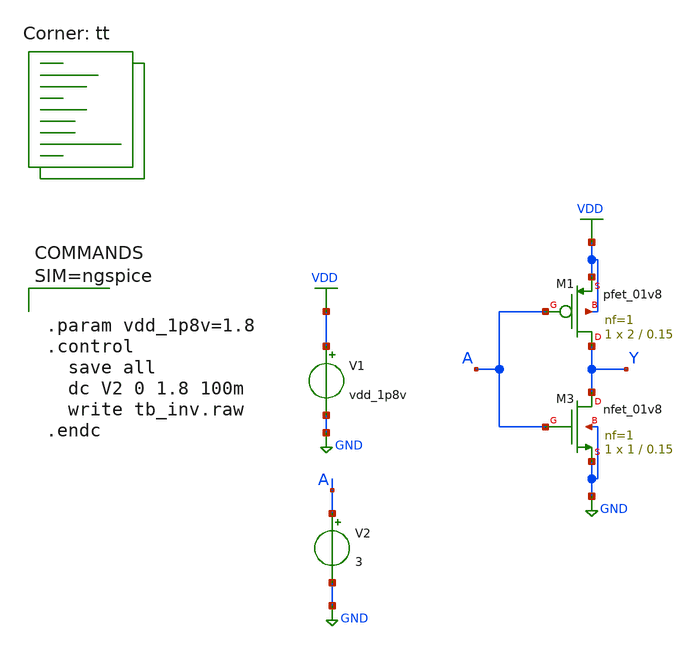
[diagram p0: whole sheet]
** sch_path: sandbox/tb_inv.sch
**.subckt tb_inv
XM3 Y A GND GND sky130_fd_pr__nfet_01v8 L=0.15 W=1 nf=1 ad='int((1 + 1)/2) * 1 / 1 * 0.29' as='int((1 + 2)/2) * 1 / 1 * 0.29'
+ pd='2*int((1 + 1)/2) * (1 / 1 + 0.29)' ps='2*int((1 + 2)/2) * (1 / 1 + 0.29)' nrd='0.29 / 1 ' nrs='0.29 / 1 '
+ sa=0 sb=0 sd=0 mult=1 m=1
XM1 Y A VDD VDD sky130_fd_pr__pfet_01v8 L=0.15 W=2 nf=1 ad='int((1 + 1)/2) * 2 / 1 * 0.29' as='int((1 + 2)/2) * 2 / 1 * 0.29'
+ pd='2*int((1 + 1)/2) * (2 / 1 + 0.29)' ps='2*int((1 + 2)/2) * (2 / 1 + 0.29)' nrd='0.29 / 2 ' nrs='0.29 / 2 '
+ sa=0 sb=0 sd=0 mult=1 m=1
V1 VDD GND vdd_1p8v
V2 A GND 3
**** begin user architecture code
.lib $::SKYWATER_MODELS/sky130.lib.spice tt



.param vdd_1p8v=1.8
.control
  save all
  dc V2 0 1.8 100m
  write tb_inv.raw
.endc



**** end user architecture code
**.ends
.GLOBAL VDD
.GLOBAL GND
.end
